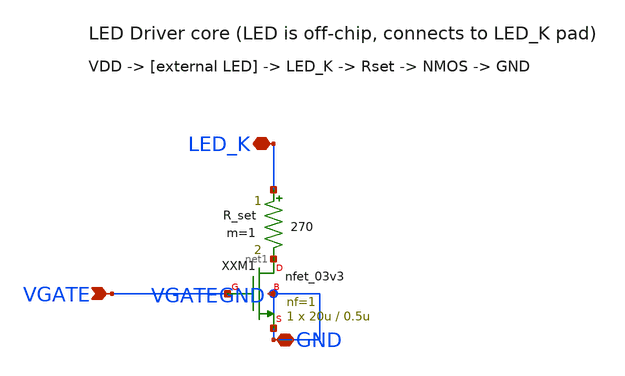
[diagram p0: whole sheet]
** sch_path: ps-led-driver/schematic/led_driver.sch
**.subckt led_driver VGATE LED_K GND
*.ipin VGATE
*.iopin LED_K
*.iopin GND
R_set LED_K net1 270 m=1
XXM1 net1 VGATE GND GND nfet_03v3 L=0.5u W=20u nf=1 ad='int((nf+1)/2) * W/nf * 0.18u' as='int((nf+2)/2) * W/nf * 0.18u'
+ pd='2*int((nf+1)/2) * (W/nf + 0.18u)' ps='2*int((nf+2)/2) * (W/nf + 0.18u)' nrd='0.18u / W' nrs='0.18u / W'
+ sa=0 sb=0 sd=0 m=1
**.ends
.end
